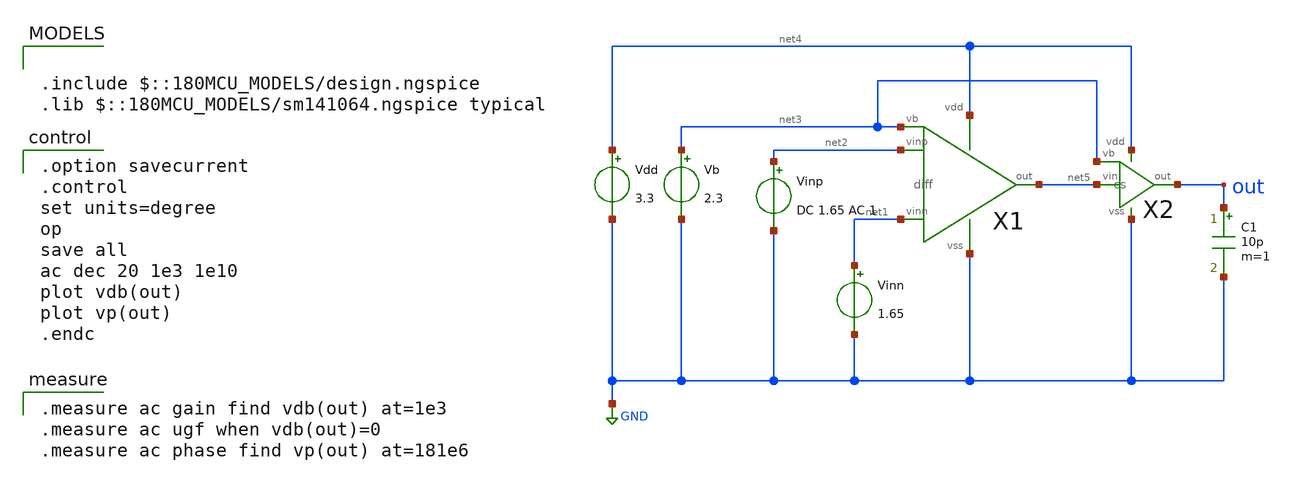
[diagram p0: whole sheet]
** sch_path: opamp/2stage_ac.sch
**.subckt 2stage_ac
Vdd net4 GND 3.3
Vb net3 GND 2.3
Vinp net2 GND DC 1.65 AC 1
X1 net2 net1 net5 net4 GND net3 diff
X2 net5 net3 out net4 GND cs
C1 out GND 10p m=1
Vinn net1 GND 1.65
**** begin user architecture code

.include $::180MCU_MODELS/design.ngspice
.lib $::180MCU_MODELS/sm141064.ngspice typical


.option savecurrent
.control
set units=degree
op
save all
ac dec 20 1e3 1e10
plot vdb(out)
plot vp(out)
.endc


.measure ac gain find vdb(out) at=1e3
.measure ac ugf when vdb(out)=0
.measure ac phase find vp(out) at=181e6

**** end user architecture code
**.ends
.GLOBAL GND
.end
